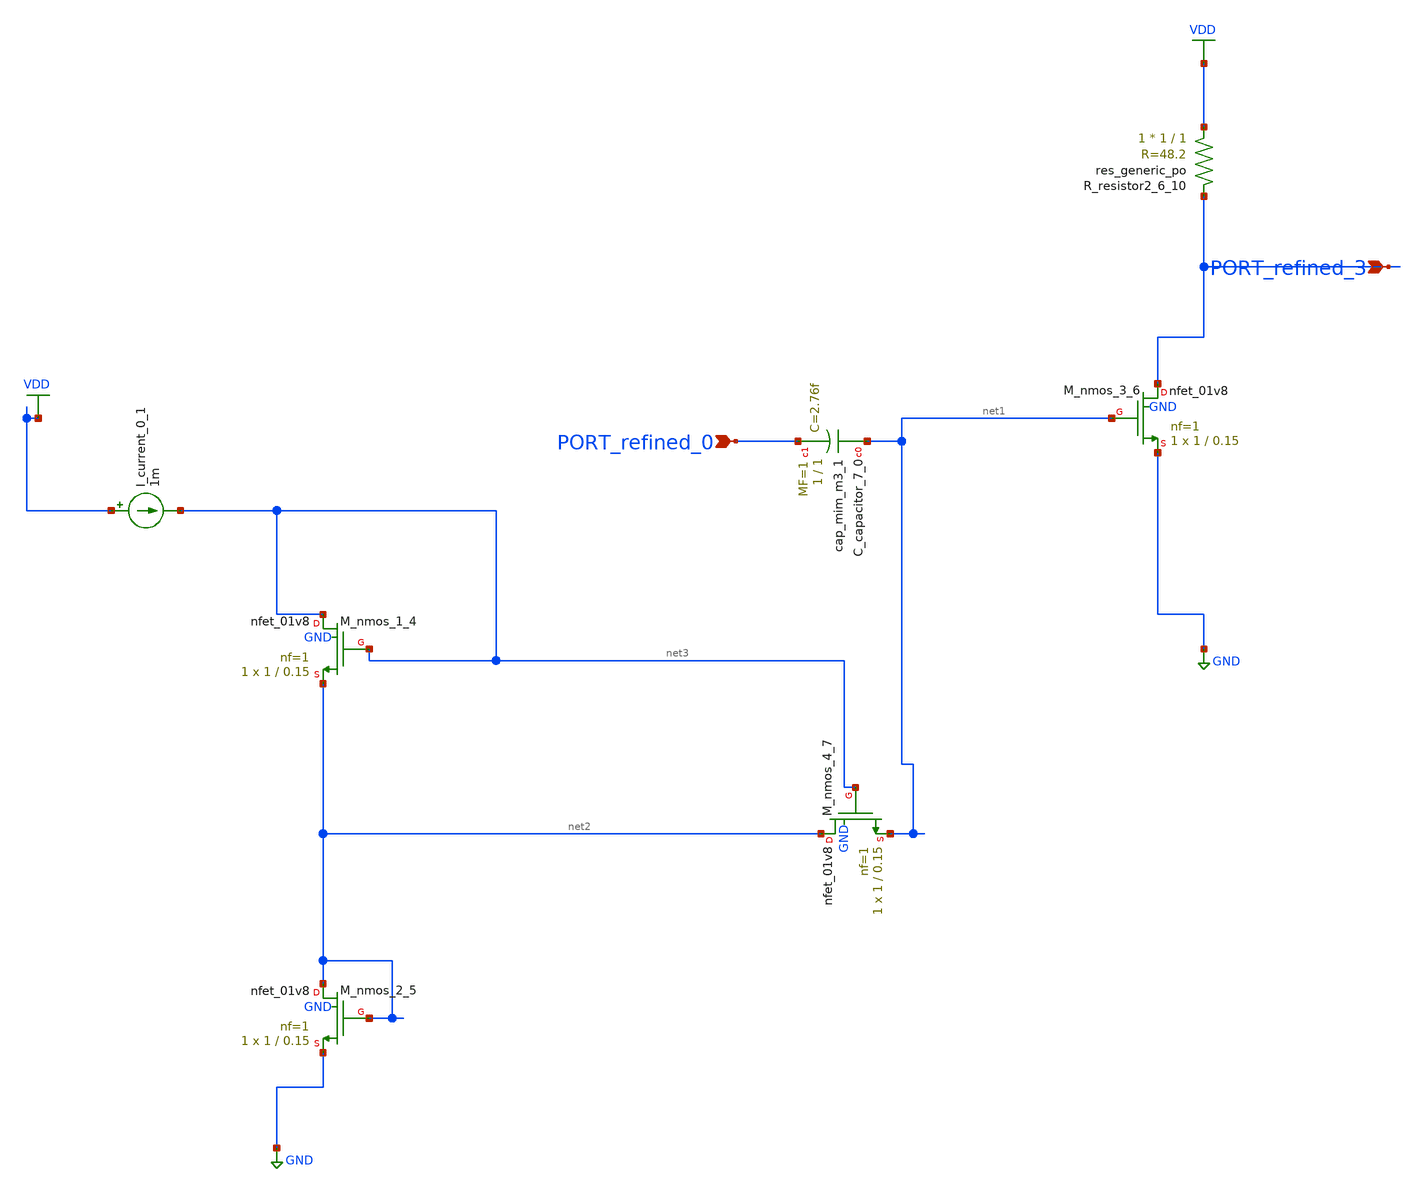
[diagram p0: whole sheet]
** sch_path: schematics/AMSNet/302.sch
**.subckt 302 PORT_refined_0 PORT_refined_3
*.ipin PORT_refined_0
*.ipin PORT_refined_3
XC_capacitor_7_0 net1 PORT_refined_0 sky130_fd_pr__cap_mim_m3_1 W=1 L=1 MF=1 m=1
I_current_0_1 VDD net3 1m
XM_nmos_1_4 net3 net3 net2 GND sky130_fd_pr__nfet_01v8 L=0.15 W=1 nf=1 ad='int((1 + 1)/2) * 1 / 1 * 0.29'
+ as='int((1 + 2)/2) * 1 / 1 * 0.29' pd='2*int((1 + 1)/2) * (1 / 1 + 0.29)' ps='2*int((1 + 2)/2) * (1 / 1 + 0.29)'
+ nrd='0.29 / 1 ' nrs='0.29 / 1 ' sa=0 sb=0 sd=0 mult=1 m=1
XM_nmos_2_5 net2 net2 GND GND sky130_fd_pr__nfet_01v8 L=0.15 W=1 nf=1 ad='int((1 + 1)/2) * 1 / 1 * 0.29'
+ as='int((1 + 2)/2) * 1 / 1 * 0.29' pd='2*int((1 + 1)/2) * (1 / 1 + 0.29)' ps='2*int((1 + 2)/2) * (1 / 1 + 0.29)'
+ nrd='0.29 / 1 ' nrs='0.29 / 1 ' sa=0 sb=0 sd=0 mult=1 m=1
XM_nmos_3_6 PORT_refined_3 net1 GND GND sky130_fd_pr__nfet_01v8 L=0.15 W=1 nf=1 ad='int((1 + 1)/2) * 1 / 1 * 0.29'
+ as='int((1 + 2)/2) * 1 / 1 * 0.29' pd='2*int((1 + 1)/2) * (1 / 1 + 0.29)' ps='2*int((1 + 2)/2) * (1 / 1 + 0.29)'
+ nrd='0.29 / 1 ' nrs='0.29 / 1 ' sa=0 sb=0 sd=0 mult=1 m=1
XM_nmos_4_7 net2 net3 net1 GND sky130_fd_pr__nfet_01v8 L=0.15 W=1 nf=1 ad='int((1 + 1)/2) * 1 / 1 * 0.29'
+ as='int((1 + 2)/2) * 1 / 1 * 0.29' pd='2*int((1 + 1)/2) * (1 / 1 + 0.29)' ps='2*int((1 + 2)/2) * (1 / 1 + 0.29)'
+ nrd='0.29 / 1 ' nrs='0.29 / 1 ' sa=0 sb=0 sd=0 mult=1 m=1
XR_resistor2_6_10 VDD PORT_refined_3 sky130_fd_pr__res_generic_po W=1 L=1 m=1
**.ends
.GLOBAL GND
.GLOBAL VDD
.end
